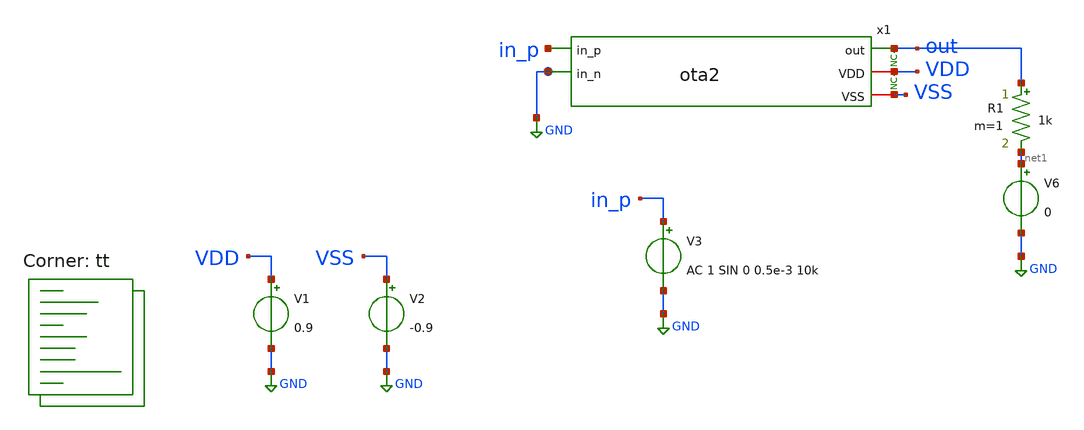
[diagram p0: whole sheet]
** sch_path: xschem/tests/ota2/ota2_ac_test.sch
**.subckt ota2_ac_test
V1 VDD GND 0.9
V2 VSS GND -0.9
V3 in_p GND AC 1 SIN 0 0.5e-3 10k
* noconn VDD
* noconn out
x1 out in_p GND VDD VSS ota2
V6 net1 GND 0
R1 out net1 1k m=1
**** begin user architecture code
.lib $::SKYWATER_MODELS/sky130.lib.spice tt
 *.lib $::SKYWATER_MODELS/sky130.lib.spice tt
.include $::SKYWATER_STDCELLS/sky130_fd_sc_hd.spice




* ngspice commands
* ngspice commands
.options list act
.options method=gear
.temp 25

.control
save all
ac dec 10 1k 10G
plot out in_p
plot i(v6)
plot i(v6)/in_p
plot i(v.x1.v1)

meas tran outptp pp v(out) from=0s to=300us
meas tran outmean avg v(out) from=0s to=300us

let gain = 20*log10($&outptp/0.002)
echo gain = $&gain

write ota2_ac_test.raw
.endc



**** end user architecture code
**.ends
.GLOBAL GND
.end
